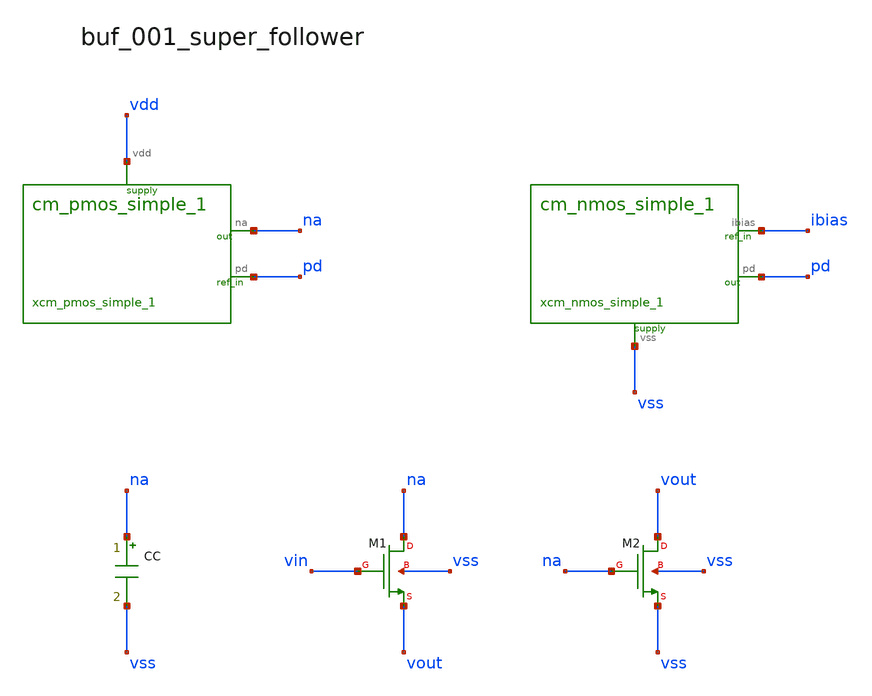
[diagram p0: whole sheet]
** sch_path: analog-db/raw/buf_001_super_follower/hier/buf_001_super_follower.sch
**.subckt buf_001_super_follower
xcm_pmos_simple_1 na pd vdd cm_pmos_simple_1
xcm_nmos_simple_1 ibias pd vss cm_nmos_simple_1
CC na vss x_cc m=1
XM1 na vin vout vss sg13_lv_nmos w=x_dut_xm1_w l=x_dut_xm1_l ng=1 m=x_dut_xm1_m
XM2 vout na vss vss sg13_lv_nmos w=x_dut_xm2_w l=x_dut_xm2_l ng=1 m=x_dut_xm2_m
**.ends

* expanding   symbol:  blocks/cm_pmos_simple_1.sym # of pins=3
** sym_path: analog-db/raw/buf_001_super_follower/hier/blocks/cm_pmos_simple_1.sym
** sch_path: analog-db/raw/buf_001_super_follower/hier/blocks/cm_pmos_simple_1.sch
.subckt cm_pmos_simple_1 na pd vdd
*.iopin vdd
*.opin pd
*.opin na
XMPB na pd vdd vdd sg13_lv_pmos w=x_dut_xmpb_w l=x_dut_xmpb_l ng=1 m=x_dut_xmpb_m
XMPD pd pd vdd vdd sg13_lv_pmos w=x_dut_xmpd_w l=x_dut_xmpd_l ng=1 m=x_dut_xmpd_m
.ends


* expanding   symbol:  blocks/cm_nmos_simple_1.sym # of pins=3
** sym_path: analog-db/raw/buf_001_super_follower/hier/blocks/cm_nmos_simple_1.sym
** sch_path: analog-db/raw/buf_001_super_follower/hier/blocks/cm_nmos_simple_1.sch
.subckt cm_nmos_simple_1 ibias pd vss
*.iopin vss
*.opin pd
*.opin ibias
XMNS pd ibias vss vss sg13_lv_nmos w=x_dut_xmns_w l=x_dut_xmns_l ng=1 m=x_dut_xmns_m
XMRN ibias ibias vss vss sg13_lv_nmos w=x_dut_xmrn_w l=x_dut_xmrn_l ng=1 m=x_dut_xmrn_m
.ends

.end
